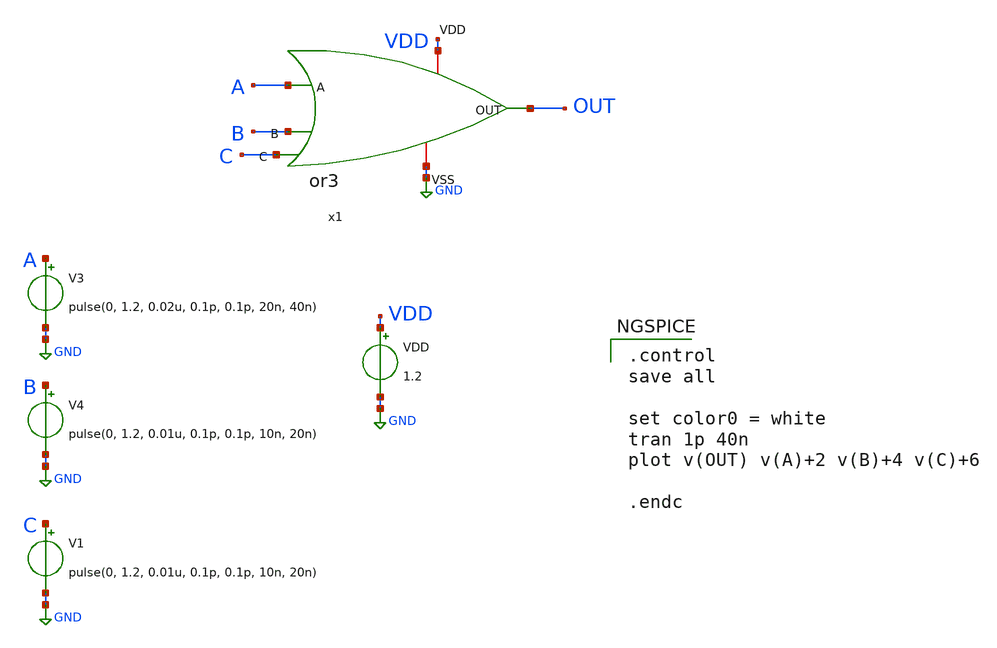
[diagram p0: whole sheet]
** sch_path: design/ALU/or3_tb.sch
**.subckt or3_tb
VDD VDD GND 1.2
V3 A GND pulse(0, 1.2, 0.02u, 0.1p, 0.1p, 20n, 40n)
V4 B GND pulse(0, 1.2, 0.01u, 0.1p, 0.1p, 10n, 20n)
x1 VDD A B C OUT GND or3
V1 C GND pulse(0, 1.2, 0.01u, 0.1p, 0.1p, 10n, 20n)
**** begin user architecture code

** opencircuitdesign pdks install
.lib $::SKYWATER_MODELS/sky130.lib.spice tt_mm



.control
save all

set color0 = white
tran 1p 40n
plot v(OUT) v(A)+2 v(B)+4 v(C)+6

.endc

**** end user architecture code
**.ends

* expanding   symbol:  or3.sym # of pins=6
** sym_path: design/OR3/xschem/or3.sym
** sch_path: design/OR3/xschem/or3.sch
.subckt or3 VDD A B C OUT VSS
*.ipin A
*.ipin B
*.iopin VSS
*.iopin VDD
*.opin OUT
*.ipin C
XM4 net1 A net3 VDD sky130_fd_pr__pfet_01v8 L=0.15 W=2.7 nf=1 ad='int((nf+1)/2) * W/nf * 0.29' as='int((nf+2)/2) * W/nf * 0.29'
+ pd='2*int((nf+1)/2) * (W/nf + 0.29)' ps='2*int((nf+2)/2) * (W/nf + 0.29)' nrd='0.29 / W' nrs='0.29 / W'
+ sa=0 sb=0 sd=0 mult=1 m=1
XM6 net2 C VDD VDD sky130_fd_pr__pfet_01v8 L=0.15 W=2.7 nf=1 ad='int((nf+1)/2) * W/nf * 0.29' as='int((nf+2)/2) * W/nf * 0.29'
+ pd='2*int((nf+1)/2) * (W/nf + 0.29)' ps='2*int((nf+2)/2) * (W/nf + 0.29)' nrd='0.29 / W' nrs='0.29 / W'
+ sa=0 sb=0 sd=0 mult=1 m=1
XM1 net1 A VSS VSS sky130_fd_pr__nfet_01v8 L=0.15 W=0.4 nf=1 ad='int((nf+1)/2) * W/nf * 0.29' as='int((nf+2)/2) * W/nf * 0.29'
+ pd='2*int((nf+1)/2) * (W/nf + 0.29)' ps='2*int((nf+2)/2) * (W/nf + 0.29)' nrd='0.29 / W' nrs='0.29 / W'
+ sa=0 sb=0 sd=0 mult=1 m=1
XM2 net1 B VSS VSS sky130_fd_pr__nfet_01v8 L=0.15 W=0.4 nf=1 ad='int((nf+1)/2) * W/nf * 0.29' as='int((nf+2)/2) * W/nf * 0.29'
+ pd='2*int((nf+1)/2) * (W/nf + 0.29)' ps='2*int((nf+2)/2) * (W/nf + 0.29)' nrd='0.29 / W' nrs='0.29 / W'
+ sa=0 sb=0 sd=0 mult=1 m=1
XM5 net3 B net2 VDD sky130_fd_pr__pfet_01v8 L=0.15 W=2.7 nf=1 ad='int((nf+1)/2) * W/nf * 0.29' as='int((nf+2)/2) * W/nf * 0.29'
+ pd='2*int((nf+1)/2) * (W/nf + 0.29)' ps='2*int((nf+2)/2) * (W/nf + 0.29)' nrd='0.29 / W' nrs='0.29 / W'
+ sa=0 sb=0 sd=0 mult=1 m=1
XM3 net1 C VSS VSS sky130_fd_pr__nfet_01v8 L=0.15 W=0.4 nf=1 ad='int((nf+1)/2) * W/nf * 0.29' as='int((nf+2)/2) * W/nf * 0.29'
+ pd='2*int((nf+1)/2) * (W/nf + 0.29)' ps='2*int((nf+2)/2) * (W/nf + 0.29)' nrd='0.29 / W' nrs='0.29 / W'
+ sa=0 sb=0 sd=0 mult=1 m=1
XM7 OUT net1 VDD VDD sky130_fd_pr__pfet_01v8 L=0.15 W=0.9 nf=1 ad='int((nf+1)/2) * W/nf * 0.29' as='int((nf+2)/2) * W/nf * 0.29'
+ pd='2*int((nf+1)/2) * (W/nf + 0.29)' ps='2*int((nf+2)/2) * (W/nf + 0.29)' nrd='0.29 / W' nrs='0.29 / W'
+ sa=0 sb=0 sd=0 mult=1 m=1
XM8 OUT net1 VSS VSS sky130_fd_pr__nfet_01v8 L=0.15 W=0.4 nf=1 ad='int((nf+1)/2) * W/nf * 0.29' as='int((nf+2)/2) * W/nf * 0.29'
+ pd='2*int((nf+1)/2) * (W/nf + 0.29)' ps='2*int((nf+2)/2) * (W/nf + 0.29)' nrd='0.29 / W' nrs='0.29 / W'
+ sa=0 sb=0 sd=0 mult=1 m=1
.ends

.GLOBAL GND
.end
